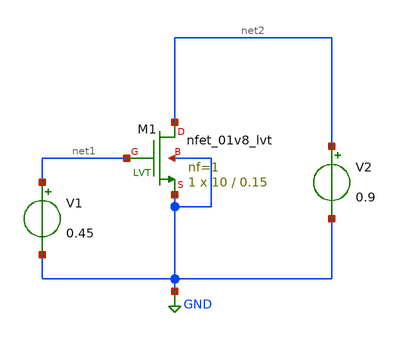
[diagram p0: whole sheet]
** sch_path: MOS-Design-Parameters/NMOS/act6_ro.sch
**.subckt act6_ro
XM1 net2 net1 GND GND sky130_fd_pr__nfet_01v8_lvt L=0.15 W=10 nf=1 ad='int((nf+1)/2) * W/nf * 0.29' as='int((nf+2)/2) * W/nf * 0.29'
+ pd='2*int((nf+1)/2) * (W/nf + 0.29)' ps='2*int((nf+2)/2) * (W/nf + 0.29)' nrd='0.29 / W' nrs='0.29 / W'
+ sa=0 sb=0 sd=0 mult=1 m=1
V1 net1 GND 0.45
V2 net2 GND 0.9
**** begin user architecture code


.lib /usr/local/share/pdk/sky130A/libs.tech/ngspice/sky130.lib.spice ss
.option wnflag=1 scale=1e-6

.control
save all

save @m.xm1.msky130_fd_pr__nfet_01v8_lvt[gds]

dc v2 0 1.8 1m

let gds = @m.xm1.msky130_fd_pr__nfet_01v8_lvt[gds]
let ro = 1/gds

#wrdata ro-ff.txt ro

.endc


**** end user architecture code
**.ends
.GLOBAL GND
.end
